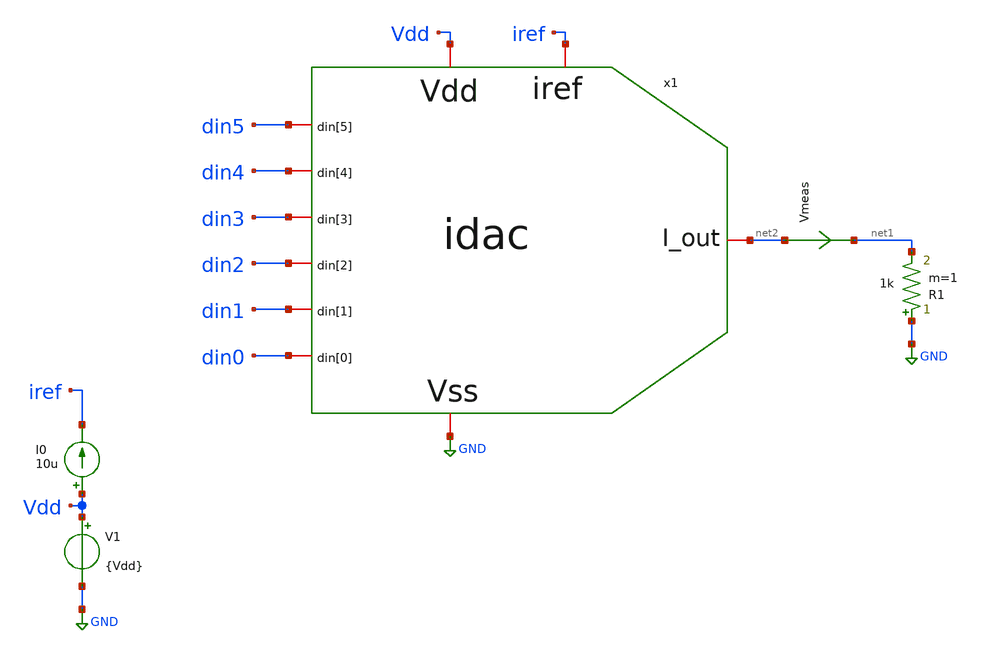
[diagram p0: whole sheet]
** sch_path: 6b_Current_DAC/design_data/xschem/Top_Tb.sch
**.subckt Top_Tb
V1 Vdd GND {Vdd}
I0 Vdd iref 10u
x1 Vdd GND iref din4 din2 din5 din1 din3 din0 net2 idac
R1 GND net1 1k m=1
Vmeas net2 net1 0
.save i(vmeas)
**** begin user architecture code


.lib cornerMOShv.lib mos_tt




*parametros de la corriente
.param wm = 1.0u
.param lm = 0.45u
.param cm = 2

.param wmp = 1.0u
.param lmp = 0.45u

.param ws = 1.0u
.param ls = 0.45u

.param Vdd = 3.3
.param Ton = 20n
.save all  @m.x1.xm7.nsg13_hv_nmos[vds]  @m.x1.xm7.nsg13_hv_nmos[id]

.tran 100p {64*Ton}

Vd0 din0 0 PULSE(0 {Vdd} {1*Ton} 100p 100p {1*Ton} {2*Ton})
Vd1 din1 0 PULSE(0 {Vdd} {2*Ton} 1100p 100p {2*Ton} {4*Ton})
Vd2 din2 0 PULSE(0 {Vdd} {4*Ton} 100p 100p {4*Ton} {8*Ton})
Vd3 din3 0 PULSE(0 {Vdd} {8*Ton} 100p 100p {8*Ton} {16*Ton})
Vd4 din4 0 PULSE(0 {Vdd} {16*Ton} 100p 100p {16*Ton} {32*Ton})
Vd5 din5 0 PULSE(0 {Vdd} {32*Ton} 100p 100p {32*Ton} {64*Ton})


.control
run
plot i(Vmeas)
write idac.raw
.endc
.end


**** end user architecture code
**.ends

* expanding   symbol:  /home/designer/shared/IHP/i_dac/xschem/idac.sym # of pins=10
** sym_path: 6b_Current_DAC/design_data/xschem/idac.sym
** sch_path: 6b_Current_DAC/design_data/xschem/idac.sch
.subckt idac Vdd Vss iref din[4] din[2] din[5] din[1] din[3] din[0] I_out
*.iopin I_out
*.iopin Vss
*.iopin iref
*.iopin Vdd
*.iopin din[0]
*.iopin din[1]
*.iopin din[2]
*.iopin din[3]
*.iopin din[4]
*.iopin din[5]
XM8 Vss iref Vgc Vss sg13_hv_nmos w={wm} l={lm} ng=1 m={cm} mm_ok=1
XM9 Vss iref iref Vss sg13_hv_nmos w={wm} l={lm} ng=1 m=1 mm_ok=1
XM10 I_out din[0] net1 Vss sg13_hv_nmos w={ws} l={ls} ng=1 m=1 mm_ok=1
XM11 I_out din[1] net3 Vss sg13_hv_nmos w={ws} l={ls} ng=1 m=2 mm_ok=1
XM12 I_out din[2] net5 Vss sg13_hv_nmos w={ws} l={ls} ng=1 m=4 mm_ok=1
XM13 I_out din[3] net8 Vss sg13_hv_nmos w={ws} l={ls} ng=1 m=8 mm_ok=1
XM14 I_out din[4] net10 Vss sg13_hv_nmos w={ws} l={ls} ng=1 m=16 mm_ok=1
XM15 I_out din[5] net12 Vss sg13_hv_nmos w={ws} l={ls} ng=1 m=32 mm_ok=1
Vmeas_1 net2 net1 0
.save i(vmeas_1)
Vmeas_2 net4 net3 0
.save i(vmeas_2)
Vmeas_3 net6 net5 0
.save i(vmeas_3)
Vmeas_4 net7 net8 0
.save i(vmeas_4)
Vmeas_5 net9 net10 0
.save i(vmeas_5)
Vmeas_6 net11 net12 0
.save i(vmeas_6)
XM1 net2 Vgc Vdd Vdd sg13_hv_pmos w={wmp} l={lmp} ng=1 m=1 mm_ok=1
XM7 Vgc Vgc Vdd Vdd sg13_hv_pmos w={wmp} l={lmp} ng=1 m=1 mm_ok=1
XM2 net4 Vgc Vdd Vdd sg13_hv_pmos w={wmp} l={lmp} ng=1 m=2 mm_ok=1
XM3 net6 Vgc Vdd Vdd sg13_hv_pmos w={wmp} l={lmp} ng=1 m=4 mm_ok=1
XM4 net7 Vgc Vdd Vdd sg13_hv_pmos w={wmp} l={lmp} ng=1 m=8 mm_ok=1
XM5 net9 Vgc Vdd Vdd sg13_hv_pmos w={wmp} l={lmp} ng=1 m=16 mm_ok=1
XM6 net11 Vgc Vdd Vdd sg13_hv_pmos w={wmp} l={lmp} ng=1 m=32 mm_ok=1
.ends

.GLOBAL GND
.end
